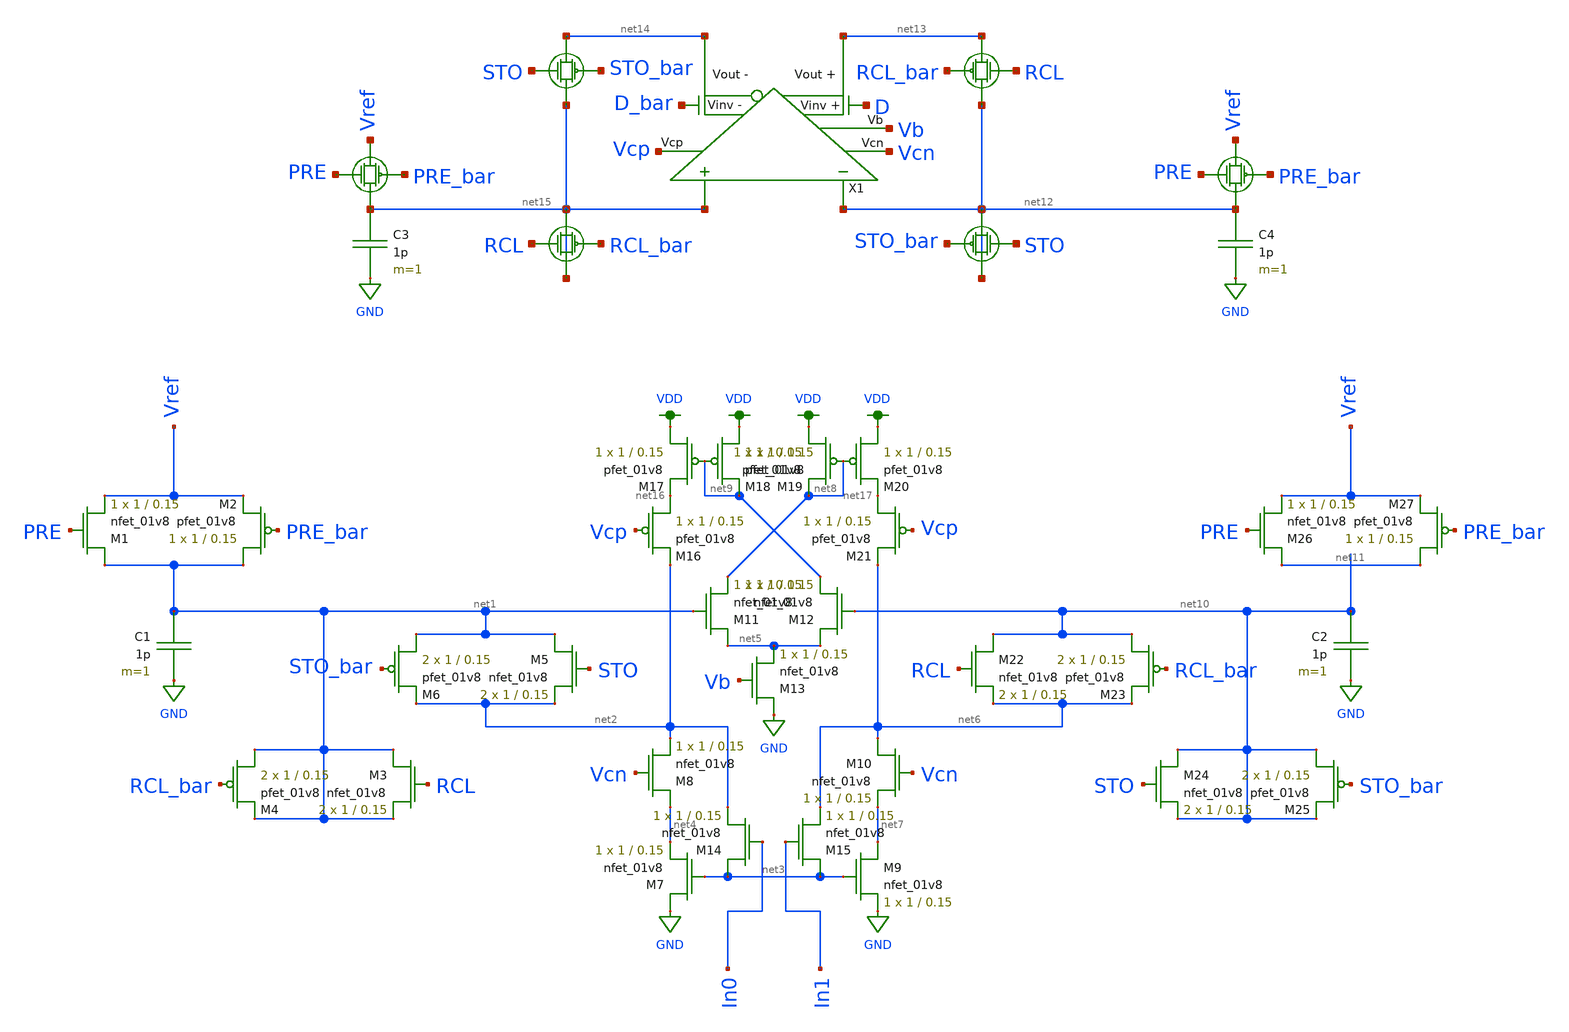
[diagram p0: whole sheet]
** sch_path: schematics/bre_example.sch
**.subckt bre_example
XM1 net1 PRE Vref GND sky130_fd_pr__nfet_01v8 L=0.15 W=1 nf=1 ad='int((nf+1)/2) * W/nf * 0.29' as='int((nf+2)/2) * W/nf * 0.29'
+ pd='2*int((nf+1)/2) * (W/nf + 0.29)' ps='2*int((nf+2)/2) * (W/nf + 0.29)' nrd='0.29 / W' nrs='0.29 / W'
+ sa=0 sb=0 sd=0 mult=1 m=1
XM2 net1 PRE_bar Vref VDD sky130_fd_pr__pfet_01v8 L=0.15 W=1 nf=1 ad='int((nf+1)/2) * W/nf * 0.29' as='int((nf+2)/2) * W/nf * 0.29'
+ pd='2*int((nf+1)/2) * (W/nf + 0.29)' ps='2*int((nf+2)/2) * (W/nf + 0.29)' nrd='0.29 / W' nrs='0.29 / W'
+ sa=0 sb=0 sd=0 mult=1 m=1
C1 net1 GND 1p m=1
XM3 net1 RCL net1 GND sky130_fd_pr__nfet_01v8 L=0.15 W=1 nf=1 ad='int((nf+1)/2) * W/nf * 0.29' as='int((nf+2)/2) * W/nf * 0.29'
+ pd='2*int((nf+1)/2) * (W/nf + 0.29)' ps='2*int((nf+2)/2) * (W/nf + 0.29)' nrd='0.29 / W' nrs='0.29 / W'
+ sa=0 sb=0 sd=0 mult=2 m=2
XM4 net1 RCL_bar net1 VDD sky130_fd_pr__pfet_01v8 L=0.15 W=1 nf=1 ad='int((nf+1)/2) * W/nf * 0.29' as='int((nf+2)/2) * W/nf * 0.29'
+ pd='2*int((nf+1)/2) * (W/nf + 0.29)' ps='2*int((nf+2)/2) * (W/nf + 0.29)' nrd='0.29 / W' nrs='0.29 / W'
+ sa=0 sb=0 sd=0 mult=2 m=2
XM7 GND net3 net4 GND sky130_fd_pr__nfet_01v8 L=0.15 W=1 nf=1 ad='int((nf+1)/2) * W/nf * 0.29' as='int((nf+2)/2) * W/nf * 0.29'
+ pd='2*int((nf+1)/2) * (W/nf + 0.29)' ps='2*int((nf+2)/2) * (W/nf + 0.29)' nrd='0.29 / W' nrs='0.29 / W'
+ sa=0 sb=0 sd=0 mult=1 m=1
XM8 net4 Vcn net2 GND sky130_fd_pr__nfet_01v8 L=0.15 W=1 nf=1 ad='int((nf+1)/2) * W/nf * 0.29' as='int((nf+2)/2) * W/nf * 0.29'
+ pd='2*int((nf+1)/2) * (W/nf + 0.29)' ps='2*int((nf+2)/2) * (W/nf + 0.29)' nrd='0.29 / W' nrs='0.29 / W'
+ sa=0 sb=0 sd=0 mult=1 m=1
XM9 net7 net3 GND GND sky130_fd_pr__nfet_01v8 L=0.15 W=1 nf=1 ad='int((nf+1)/2) * W/nf * 0.29' as='int((nf+2)/2) * W/nf * 0.29'
+ pd='2*int((nf+1)/2) * (W/nf + 0.29)' ps='2*int((nf+2)/2) * (W/nf + 0.29)' nrd='0.29 / W' nrs='0.29 / W'
+ sa=0 sb=0 sd=0 mult=1 m=1
XM10 net6 Vcn net7 GND sky130_fd_pr__nfet_01v8 L=0.15 W=1 nf=1 ad='int((nf+1)/2) * W/nf * 0.29' as='int((nf+2)/2) * W/nf * 0.29'
+ pd='2*int((nf+1)/2) * (W/nf + 0.29)' ps='2*int((nf+2)/2) * (W/nf + 0.29)' nrd='0.29 / W' nrs='0.29 / W'
+ sa=0 sb=0 sd=0 mult=1 m=1
XM11 net5 net1 net8 GND sky130_fd_pr__nfet_01v8 L=0.15 W=1 nf=1 ad='int((nf+1)/2) * W/nf * 0.29' as='int((nf+2)/2) * W/nf * 0.29'
+ pd='2*int((nf+1)/2) * (W/nf + 0.29)' ps='2*int((nf+2)/2) * (W/nf + 0.29)' nrd='0.29 / W' nrs='0.29 / W'
+ sa=0 sb=0 sd=0 mult=1 m=1
XM12 net5 net10 net9 GND sky130_fd_pr__nfet_01v8 L=0.15 W=1 nf=1 ad='int((nf+1)/2) * W/nf * 0.29' as='int((nf+2)/2) * W/nf * 0.29'
+ pd='2*int((nf+1)/2) * (W/nf + 0.29)' ps='2*int((nf+2)/2) * (W/nf + 0.29)' nrd='0.29 / W' nrs='0.29 / W'
+ sa=0 sb=0 sd=0 mult=1 m=1
XM13 GND Vb net5 GND sky130_fd_pr__nfet_01v8 L=0.15 W=1 nf=1 ad='int((nf+1)/2) * W/nf * 0.29' as='int((nf+2)/2) * W/nf * 0.29'
+ pd='2*int((nf+1)/2) * (W/nf + 0.29)' ps='2*int((nf+2)/2) * (W/nf + 0.29)' nrd='0.29 / W' nrs='0.29 / W'
+ sa=0 sb=0 sd=0 mult=1 m=1
XM14 net3 In0 net2 GND sky130_fd_pr__nfet_01v8 L=0.15 W=1 nf=1 ad='int((nf+1)/2) * W/nf * 0.29' as='int((nf+2)/2) * W/nf * 0.29'
+ pd='2*int((nf+1)/2) * (W/nf + 0.29)' ps='2*int((nf+2)/2) * (W/nf + 0.29)' nrd='0.29 / W' nrs='0.29 / W'
+ sa=0 sb=0 sd=0 mult=1 m=1
XM15 net3 In1 net6 GND sky130_fd_pr__nfet_01v8 L=0.15 W=1 nf=1 ad='int((nf+1)/2) * W/nf * 0.29' as='int((nf+2)/2) * W/nf * 0.29'
+ pd='2*int((nf+1)/2) * (W/nf + 0.29)' ps='2*int((nf+2)/2) * (W/nf + 0.29)' nrd='0.29 / W' nrs='0.29 / W'
+ sa=0 sb=0 sd=0 mult=1 m=1
XM16 net16 Vcp net2 VDD sky130_fd_pr__pfet_01v8 L=0.15 W=1 nf=1 ad='int((nf+1)/2) * W/nf * 0.29' as='int((nf+2)/2) * W/nf * 0.29'
+ pd='2*int((nf+1)/2) * (W/nf + 0.29)' ps='2*int((nf+2)/2) * (W/nf + 0.29)' nrd='0.29 / W' nrs='0.29 / W'
+ sa=0 sb=0 sd=0 mult=1 m=1
XM17 VDD net9 net16 VDD sky130_fd_pr__pfet_01v8 L=0.15 W=1 nf=1 ad='int((nf+1)/2) * W/nf * 0.29' as='int((nf+2)/2) * W/nf * 0.29'
+ pd='2*int((nf+1)/2) * (W/nf + 0.29)' ps='2*int((nf+2)/2) * (W/nf + 0.29)' nrd='0.29 / W' nrs='0.29 / W'
+ sa=0 sb=0 sd=0 mult=1 m=1
XM18 VDD net9 net9 VDD sky130_fd_pr__pfet_01v8 L=0.15 W=1 nf=1 ad='int((nf+1)/2) * W/nf * 0.29' as='int((nf+2)/2) * W/nf * 0.29'
+ pd='2*int((nf+1)/2) * (W/nf + 0.29)' ps='2*int((nf+2)/2) * (W/nf + 0.29)' nrd='0.29 / W' nrs='0.29 / W'
+ sa=0 sb=0 sd=0 mult=1 m=1
XM19 VDD net8 net8 VDD sky130_fd_pr__pfet_01v8 L=0.15 W=1 nf=1 ad='int((nf+1)/2) * W/nf * 0.29' as='int((nf+2)/2) * W/nf * 0.29'
+ pd='2*int((nf+1)/2) * (W/nf + 0.29)' ps='2*int((nf+2)/2) * (W/nf + 0.29)' nrd='0.29 / W' nrs='0.29 / W'
+ sa=0 sb=0 sd=0 mult=1 m=1
XM20 VDD net8 net17 VDD sky130_fd_pr__pfet_01v8 L=0.15 W=1 nf=1 ad='int((nf+1)/2) * W/nf * 0.29' as='int((nf+2)/2) * W/nf * 0.29'
+ pd='2*int((nf+1)/2) * (W/nf + 0.29)' ps='2*int((nf+2)/2) * (W/nf + 0.29)' nrd='0.29 / W' nrs='0.29 / W'
+ sa=0 sb=0 sd=0 mult=1 m=1
XM21 net17 Vcp net6 VDD sky130_fd_pr__pfet_01v8 L=0.15 W=1 nf=1 ad='int((nf+1)/2) * W/nf * 0.29' as='int((nf+2)/2) * W/nf * 0.29'
+ pd='2*int((nf+1)/2) * (W/nf + 0.29)' ps='2*int((nf+2)/2) * (W/nf + 0.29)' nrd='0.29 / W' nrs='0.29 / W'
+ sa=0 sb=0 sd=0 mult=1 m=1
XM26 net11 PRE Vref GND sky130_fd_pr__nfet_01v8 L=0.15 W=1 nf=1 ad='int((nf+1)/2) * W/nf * 0.29' as='int((nf+2)/2) * W/nf * 0.29'
+ pd='2*int((nf+1)/2) * (W/nf + 0.29)' ps='2*int((nf+2)/2) * (W/nf + 0.29)' nrd='0.29 / W' nrs='0.29 / W'
+ sa=0 sb=0 sd=0 mult=1 m=1
XM27 net11 PRE_bar Vref VDD sky130_fd_pr__pfet_01v8 L=0.15 W=1 nf=1 ad='int((nf+1)/2) * W/nf * 0.29'
+ as='int((nf+2)/2) * W/nf * 0.29' pd='2*int((nf+1)/2) * (W/nf + 0.29)' ps='2*int((nf+2)/2) * (W/nf + 0.29)'
+ nrd='0.29 / W' nrs='0.29 / W' sa=0 sb=0 sd=0 mult=1 m=1
C2 net10 GND 1p m=1
XM5 net1 STO net2 GND sky130_fd_pr__nfet_01v8 L=0.15 W=1 nf=1 ad='int((nf+1)/2) * W/nf * 0.29' as='int((nf+2)/2) * W/nf * 0.29'
+ pd='2*int((nf+1)/2) * (W/nf + 0.29)' ps='2*int((nf+2)/2) * (W/nf + 0.29)' nrd='0.29 / W' nrs='0.29 / W'
+ sa=0 sb=0 sd=0 mult=2 m=2
XM22 net10 RCL net6 GND sky130_fd_pr__nfet_01v8 L=0.15 W=1 nf=1 ad='int((nf+1)/2) * W/nf * 0.29' as='int((nf+2)/2) * W/nf * 0.29'
+ pd='2*int((nf+1)/2) * (W/nf + 0.29)' ps='2*int((nf+2)/2) * (W/nf + 0.29)' nrd='0.29 / W' nrs='0.29 / W'
+ sa=0 sb=0 sd=0 mult=2 m=2
XM24 net10 STO net10 GND sky130_fd_pr__nfet_01v8 L=0.15 W=1 nf=1 ad='int((nf+1)/2) * W/nf * 0.29' as='int((nf+2)/2) * W/nf * 0.29'
+ pd='2*int((nf+1)/2) * (W/nf + 0.29)' ps='2*int((nf+2)/2) * (W/nf + 0.29)' nrd='0.29 / W' nrs='0.29 / W'
+ sa=0 sb=0 sd=0 mult=2 m=2
XM6 net1 STO_bar net2 VDD sky130_fd_pr__pfet_01v8 L=0.15 W=1 nf=1 ad='int((nf+1)/2) * W/nf * 0.29' as='int((nf+2)/2) * W/nf * 0.29'
+ pd='2*int((nf+1)/2) * (W/nf + 0.29)' ps='2*int((nf+2)/2) * (W/nf + 0.29)' nrd='0.29 / W' nrs='0.29 / W'
+ sa=0 sb=0 sd=0 mult=2 m=2
XM23 net10 RCL_bar net6 VDD sky130_fd_pr__pfet_01v8 L=0.15 W=1 nf=1 ad='int((nf+1)/2) * W/nf * 0.29'
+ as='int((nf+2)/2) * W/nf * 0.29' pd='2*int((nf+1)/2) * (W/nf + 0.29)' ps='2*int((nf+2)/2) * (W/nf + 0.29)'
+ nrd='0.29 / W' nrs='0.29 / W' sa=0 sb=0 sd=0 mult=2 m=2
XM25 net10 STO_bar net10 VDD sky130_fd_pr__pfet_01v8 L=0.15 W=1 nf=1 ad='int((nf+1)/2) * W/nf * 0.29'
+ as='int((nf+2)/2) * W/nf * 0.29' pd='2*int((nf+1)/2) * (W/nf + 0.29)' ps='2*int((nf+2)/2) * (W/nf + 0.29)'
+ nrd='0.29 / W' nrs='0.29 / W' sa=0 sb=0 sd=0 mult=2 m=2
X1 D_bar net13 net14 Vcp Vb net12 net15 D Vcn ota W_U=12 L_U=0.5
C4 net12 GND 1p m=1
C3 net15 GND 1p m=1
**.ends

* expanding   symbol:  ../schematics/ota.sym # of pins=9
** sym_path: schematics/ota.sym
** sch_path: schematics/ota.sch
.subckt ota Vinv_n Vout_p Vout_n Vcp Vb Vin_n Vin_p Vinv_p Vcn  L_U=0.5 W_U=12
*.ipin Vin_n
*.ipin Vin_p
*.opin Vout_n
*.opin Vout_p
*.ipin Vcp
*.ipin Vb
*.ipin Vinv_p
*.ipin Vinv_n
*.ipin Vcn
XM18 net3 net3 VDD VDD sky130_fd_pr__pfet_01v8 L=L_U W=W_U nf=1 ad='int((nf+1)/2) * W/nf * 0.29' as='int((nf+2)/2) * W/nf * 0.29'
+ pd='2*int((nf+1)/2) * (W/nf + 0.29)' ps='2*int((nf+2)/2) * (W/nf + 0.29)' nrd='0.29 / W' nrs='0.29 / W'
+ sa=0 sb=0 sd=0 mult=1 m=1
XM19 net4 Vin_n net1 GND sky130_fd_pr__nfet_01v8 L=L_U W=W_U nf=1 ad='int((nf+1)/2) * W/nf * 0.29' as='int((nf+2)/2) * W/nf * 0.29'
+ pd='2*int((nf+1)/2) * (W/nf + 0.29)' ps='2*int((nf+2)/2) * (W/nf + 0.29)' nrd='0.29 / W' nrs='0.29 / W'
+ sa=0 sb=0 sd=0 mult=1 m=1
XM20 net3 Vin_p net1 GND sky130_fd_pr__nfet_01v8 L=L_U W=W_U nf=1 ad='int((nf+1)/2) * W/nf * 0.29' as='int((nf+2)/2) * W/nf * 0.29'
+ pd='2*int((nf+1)/2) * (W/nf + 0.29)' ps='2*int((nf+2)/2) * (W/nf + 0.29)' nrd='0.29 / W' nrs='0.29 / W'
+ sa=0 sb=0 sd=0 mult=1 m=1
XM21 net1 Vb GND GND sky130_fd_pr__nfet_01v8 L=L_U W=W_U nf=1 ad='int((nf+1)/2) * W/nf * 0.29' as='int((nf+2)/2) * W/nf * 0.29'
+ pd='2*int((nf+1)/2) * (W/nf + 0.29)' ps='2*int((nf+2)/2) * (W/nf + 0.29)' nrd='0.29 / W' nrs='0.29 / W'
+ sa=0 sb=0 sd=0 mult=1 m=1
XM22 net4 net4 VDD VDD sky130_fd_pr__pfet_01v8 L=L_U W=W_U nf=1 ad='int((nf+1)/2) * W/nf * 0.29' as='int((nf+2)/2) * W/nf * 0.29'
+ pd='2*int((nf+1)/2) * (W/nf + 0.29)' ps='2*int((nf+2)/2) * (W/nf + 0.29)' nrd='0.29 / W' nrs='0.29 / W'
+ sa=0 sb=0 sd=0 mult=1 m=1
XM23 net7 net3 VDD VDD sky130_fd_pr__pfet_01v8 L=L_U W=W_U nf=1 ad='int((nf+1)/2) * W/nf * 0.29' as='int((nf+2)/2) * W/nf * 0.29'
+ pd='2*int((nf+1)/2) * (W/nf + 0.29)' ps='2*int((nf+2)/2) * (W/nf + 0.29)' nrd='0.29 / W' nrs='0.29 / W'
+ sa=0 sb=0 sd=0 mult=1 m=1
XM24 net8 net4 VDD VDD sky130_fd_pr__pfet_01v8 L=L_U W=W_U nf=1 ad='int((nf+1)/2) * W/nf * 0.29' as='int((nf+2)/2) * W/nf * 0.29'
+ pd='2*int((nf+1)/2) * (W/nf + 0.29)' ps='2*int((nf+2)/2) * (W/nf + 0.29)' nrd='0.29 / W' nrs='0.29 / W'
+ sa=0 sb=0 sd=0 mult=1 m=1
XM25 net8 Vcp Vout_n VDD sky130_fd_pr__pfet_01v8 L=L_U W=W_U nf=1 ad='int((nf+1)/2) * W/nf * 0.29' as='int((nf+2)/2) * W/nf * 0.29'
+ pd='2*int((nf+1)/2) * (W/nf + 0.29)' ps='2*int((nf+2)/2) * (W/nf + 0.29)' nrd='0.29 / W' nrs='0.29 / W'
+ sa=0 sb=0 sd=0 mult=1 m=1
XM26 Vout_p Vcp net7 VDD sky130_fd_pr__pfet_01v8 L=L_U W=W_U nf=1 ad='int((nf+1)/2) * W/nf * 0.29' as='int((nf+2)/2) * W/nf * 0.29'
+ pd='2*int((nf+1)/2) * (W/nf + 0.29)' ps='2*int((nf+2)/2) * (W/nf + 0.29)' nrd='0.29 / W' nrs='0.29 / W'
+ sa=0 sb=0 sd=0 mult=1 m=1
XM27 Vout_p Vcn net6 GND sky130_fd_pr__nfet_01v8 L=L_U W=W_U nf=1 ad='int((nf+1)/2) * W/nf * 0.29' as='int((nf+2)/2) * W/nf * 0.29'
+ pd='2*int((nf+1)/2) * (W/nf + 0.29)' ps='2*int((nf+2)/2) * (W/nf + 0.29)' nrd='0.29 / W' nrs='0.29 / W'
+ sa=0 sb=0 sd=0 mult=1 m=1
XM28 Vout_n Vcn net2 GND sky130_fd_pr__nfet_01v8 L=L_U W=W_U nf=1 ad='int((nf+1)/2) * W/nf * 0.29' as='int((nf+2)/2) * W/nf * 0.29'
+ pd='2*int((nf+1)/2) * (W/nf + 0.29)' ps='2*int((nf+2)/2) * (W/nf + 0.29)' nrd='0.29 / W' nrs='0.29 / W'
+ sa=0 sb=0 sd=0 mult=1 m=1
XM29 net6 net5 GND GND sky130_fd_pr__nfet_01v8 L=L_U W=W_U nf=1 ad='int((nf+1)/2) * W/nf * 0.29' as='int((nf+2)/2) * W/nf * 0.29'
+ pd='2*int((nf+1)/2) * (W/nf + 0.29)' ps='2*int((nf+2)/2) * (W/nf + 0.29)' nrd='0.29 / W' nrs='0.29 / W'
+ sa=0 sb=0 sd=0 mult=1 m=1
XM30 Vout_p Vinv_p net5 GND sky130_fd_pr__nfet_01v8 L=L_U W=W_U nf=1 ad='int((nf+1)/2) * W/nf * 0.29'
+ as='int((nf+2)/2) * W/nf * 0.29' pd='2*int((nf+1)/2) * (W/nf + 0.29)' ps='2*int((nf+2)/2) * (W/nf + 0.29)'
+ nrd='0.29 / W' nrs='0.29 / W' sa=0 sb=0 sd=0 mult=1 m=1
XM32 net2 net5 GND GND sky130_fd_pr__nfet_01v8 L=L_U W=W_U nf=1 ad='int((nf+1)/2) * W/nf * 0.29' as='int((nf+2)/2) * W/nf * 0.29'
+ pd='2*int((nf+1)/2) * (W/nf + 0.29)' ps='2*int((nf+2)/2) * (W/nf + 0.29)' nrd='0.29 / W' nrs='0.29 / W'
+ sa=0 sb=0 sd=0 mult=1 m=1
XM34 Vout_n Vinv_n net5 GND sky130_fd_pr__nfet_01v8 L=L_U W=W_U nf=1 ad='int((nf+1)/2) * W/nf * 0.29'
+ as='int((nf+2)/2) * W/nf * 0.29' pd='2*int((nf+1)/2) * (W/nf + 0.29)' ps='2*int((nf+2)/2) * (W/nf + 0.29)'
+ nrd='0.29 / W' nrs='0.29 / W' sa=0 sb=0 sd=0 mult=1 m=1
.ends

.GLOBAL GND
.GLOBAL VDD
.end
